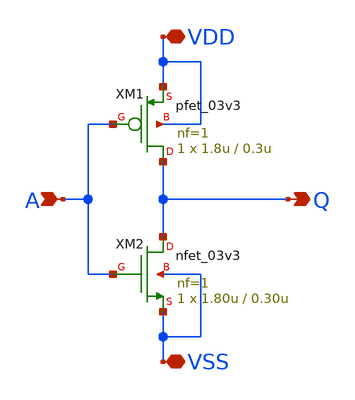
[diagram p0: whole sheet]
** sch_path: work/inverter_20261112/inv_dut_113.sch
**.subckt inv_dut_113 A Q VSS VDD
*.ipin A
*.opin Q
*.iopin VSS
*.iopin VDD
XM2 Q A VSS VSS nfet_03v3 L=0.30u W=1.80u nf=1 ad='int((nf+1)/2) * W/nf * 0.18u' as='int((nf+2)/2) * W/nf * 0.18u'
+ pd='2*int((nf+1)/2) * (W/nf + 0.18u)' ps='2*int((nf+2)/2) * (W/nf + 0.18u)' nrd='0.18u / W' nrs='0.18u / W'
+ sa=0 sb=0 sd=0 m=1
XM1 Q A VDD VDD pfet_03v3 L=0.3u W=1.8u nf=1 ad='int((nf+1)/2) * W/nf * 0.18u' as='int((nf+2)/2) * W/nf * 0.18u'
+ pd='2*int((nf+1)/2) * (W/nf + 0.18u)' ps='2*int((nf+2)/2) * (W/nf + 0.18u)' nrd='0.18u / W' nrs='0.18u / W'
+ sa=0 sb=0 sd=0 m=1
**.ends
.end
